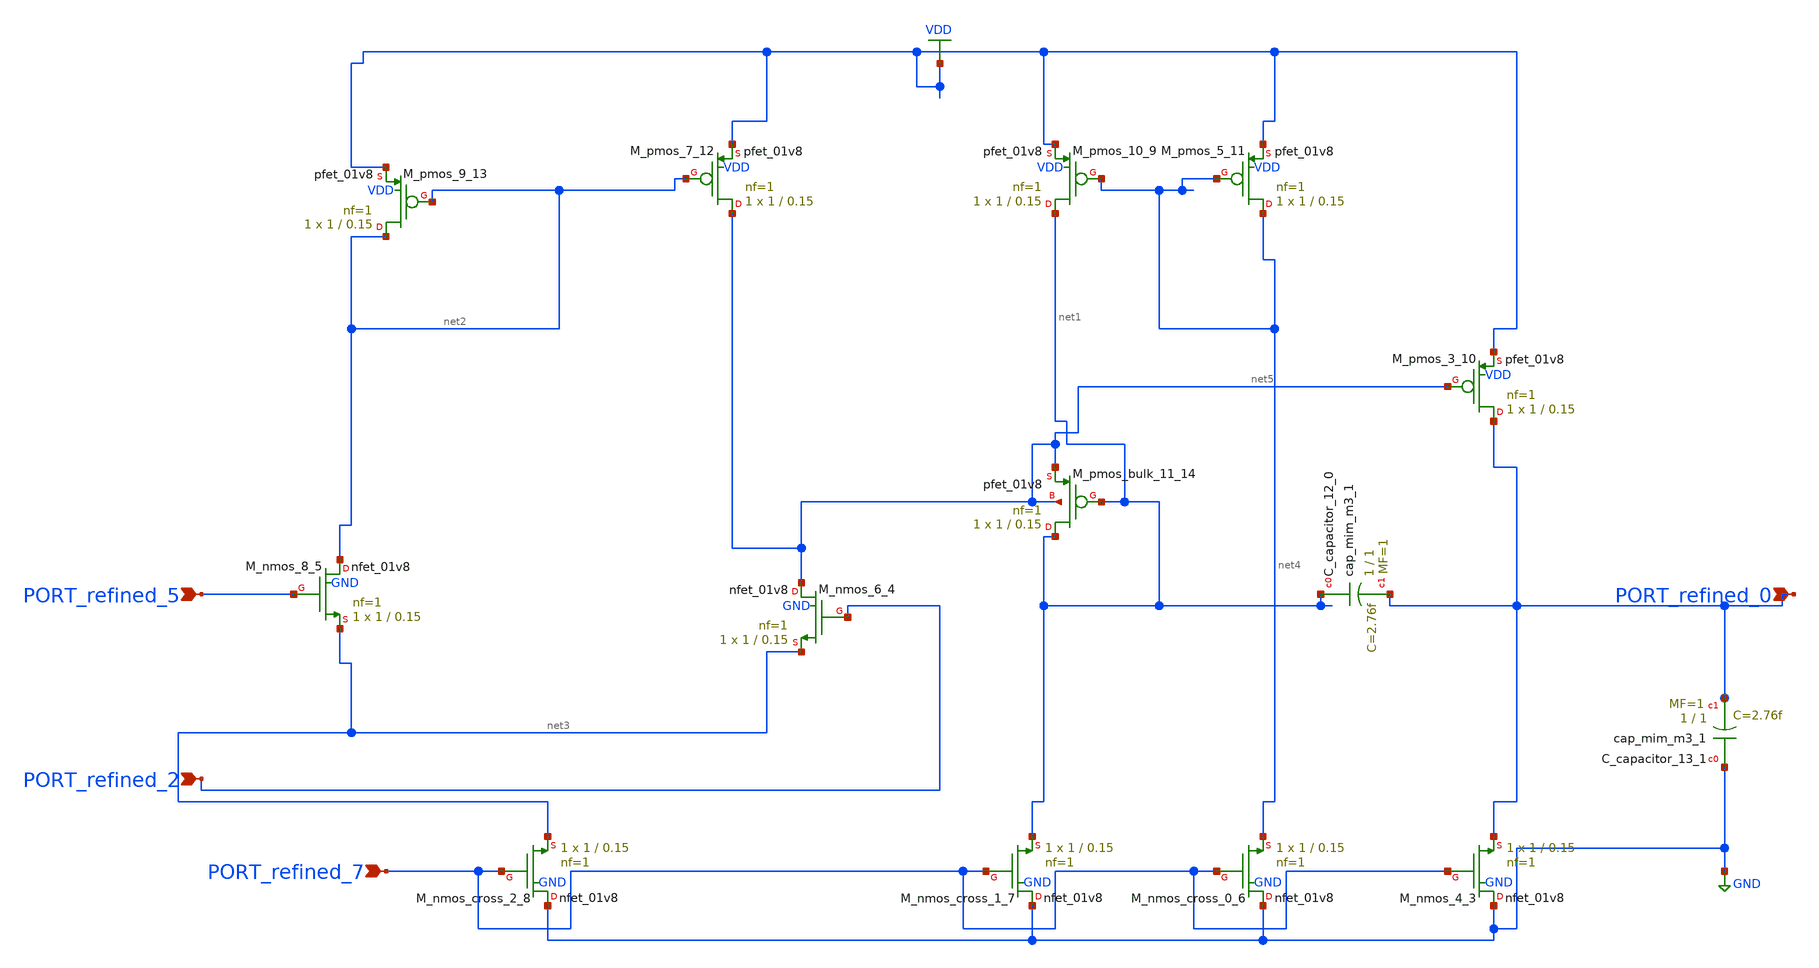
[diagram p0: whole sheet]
** sch_path: schematics/Image2Net/070.sch
**.subckt 070 PORT_refined_0 PORT_refined_2 PORT_refined_5 PORT_refined_7
*.ipin PORT_refined_0
*.ipin PORT_refined_2
*.ipin PORT_refined_5
*.ipin PORT_refined_7
XC_capacitor_12_0 net1 PORT_refined_0 sky130_fd_pr__cap_mim_m3_1 W=1 L=1 MF=1 m=1
XC_capacitor_13_1 GND PORT_refined_0 sky130_fd_pr__cap_mim_m3_1 W=1 L=1 MF=1 m=1
XM_nmos_4_3 GND PORT_refined_7 PORT_refined_0 GND sky130_fd_pr__nfet_01v8 L=0.15 W=1 nf=1 ad='int((1 + 1)/2) * 1 / 1 * 0.29'
+ as='int((1 + 2)/2) * 1 / 1 * 0.29' pd='2*int((1 + 1)/2) * (1 / 1 + 0.29)' ps='2*int((1 + 2)/2) * (1 / 1 + 0.29)'
+ nrd='0.29 / 1 ' nrs='0.29 / 1 ' sa=0 sb=0 sd=0 mult=1 m=1
XM_nmos_6_4 net5 PORT_refined_2 net3 GND sky130_fd_pr__nfet_01v8 L=0.15 W=1 nf=1 ad='int((1 + 1)/2) * 1 / 1 * 0.29'
+ as='int((1 + 2)/2) * 1 / 1 * 0.29' pd='2*int((1 + 1)/2) * (1 / 1 + 0.29)' ps='2*int((1 + 2)/2) * (1 / 1 + 0.29)'
+ nrd='0.29 / 1 ' nrs='0.29 / 1 ' sa=0 sb=0 sd=0 mult=1 m=1
XM_nmos_8_5 net2 PORT_refined_5 net3 GND sky130_fd_pr__nfet_01v8 L=0.15 W=1 nf=1 ad='int((1 + 1)/2) * 1 / 1 * 0.29'
+ as='int((1 + 2)/2) * 1 / 1 * 0.29' pd='2*int((1 + 1)/2) * (1 / 1 + 0.29)' ps='2*int((1 + 2)/2) * (1 / 1 + 0.29)'
+ nrd='0.29 / 1 ' nrs='0.29 / 1 ' sa=0 sb=0 sd=0 mult=1 m=1
XM_nmos_cross_0_6 GND PORT_refined_7 net4 GND sky130_fd_pr__nfet_01v8 L=0.15 W=1 nf=1 ad='int((1 + 1)/2) * 1 / 1 * 0.29'
+ as='int((1 + 2)/2) * 1 / 1 * 0.29' pd='2*int((1 + 1)/2) * (1 / 1 + 0.29)' ps='2*int((1 + 2)/2) * (1 / 1 + 0.29)'
+ nrd='0.29 / 1 ' nrs='0.29 / 1 ' sa=0 sb=0 sd=0 mult=1 m=1
XM_nmos_cross_1_7 GND PORT_refined_7 net1 GND sky130_fd_pr__nfet_01v8 L=0.15 W=1 nf=1 ad='int((1 + 1)/2) * 1 / 1 * 0.29'
+ as='int((1 + 2)/2) * 1 / 1 * 0.29' pd='2*int((1 + 1)/2) * (1 / 1 + 0.29)' ps='2*int((1 + 2)/2) * (1 / 1 + 0.29)'
+ nrd='0.29 / 1 ' nrs='0.29 / 1 ' sa=0 sb=0 sd=0 mult=1 m=1
XM_nmos_cross_2_8 GND PORT_refined_7 net3 GND sky130_fd_pr__nfet_01v8 L=0.15 W=1 nf=1 ad='int((1 + 1)/2) * 1 / 1 * 0.29'
+ as='int((1 + 2)/2) * 1 / 1 * 0.29' pd='2*int((1 + 1)/2) * (1 / 1 + 0.29)' ps='2*int((1 + 2)/2) * (1 / 1 + 0.29)'
+ nrd='0.29 / 1 ' nrs='0.29 / 1 ' sa=0 sb=0 sd=0 mult=1 m=1
XM_pmos_10_9 net1 net4 VDD VDD sky130_fd_pr__pfet_01v8 L=0.15 W=1 nf=1 ad='int((1 + 1)/2) * 1 / 1 * 0.29'
+ as='int((1 + 2)/2) * 1 / 1 * 0.29' pd='2*int((1 + 1)/2) * (1 / 1 + 0.29)' ps='2*int((1 + 2)/2) * (1 / 1 + 0.29)'
+ nrd='0.29 / 1 ' nrs='0.29 / 1 ' sa=0 sb=0 sd=0 mult=1 m=1
XM_pmos_3_10 PORT_refined_0 net5 VDD VDD sky130_fd_pr__pfet_01v8 L=0.15 W=1 nf=1 ad='int((1 + 1)/2) * 1 / 1 * 0.29'
+ as='int((1 + 2)/2) * 1 / 1 * 0.29' pd='2*int((1 + 1)/2) * (1 / 1 + 0.29)' ps='2*int((1 + 2)/2) * (1 / 1 + 0.29)'
+ nrd='0.29 / 1 ' nrs='0.29 / 1 ' sa=0 sb=0 sd=0 mult=1 m=1
XM_pmos_5_11 net4 net4 VDD VDD sky130_fd_pr__pfet_01v8 L=0.15 W=1 nf=1 ad='int((1 + 1)/2) * 1 / 1 * 0.29'
+ as='int((1 + 2)/2) * 1 / 1 * 0.29' pd='2*int((1 + 1)/2) * (1 / 1 + 0.29)' ps='2*int((1 + 2)/2) * (1 / 1 + 0.29)'
+ nrd='0.29 / 1 ' nrs='0.29 / 1 ' sa=0 sb=0 sd=0 mult=1 m=1
XM_pmos_7_12 net5 net2 VDD VDD sky130_fd_pr__pfet_01v8 L=0.15 W=1 nf=1 ad='int((1 + 1)/2) * 1 / 1 * 0.29'
+ as='int((1 + 2)/2) * 1 / 1 * 0.29' pd='2*int((1 + 1)/2) * (1 / 1 + 0.29)' ps='2*int((1 + 2)/2) * (1 / 1 + 0.29)'
+ nrd='0.29 / 1 ' nrs='0.29 / 1 ' sa=0 sb=0 sd=0 mult=1 m=1
XM_pmos_9_13 net2 net2 VDD VDD sky130_fd_pr__pfet_01v8 L=0.15 W=1 nf=1 ad='int((1 + 1)/2) * 1 / 1 * 0.29'
+ as='int((1 + 2)/2) * 1 / 1 * 0.29' pd='2*int((1 + 1)/2) * (1 / 1 + 0.29)' ps='2*int((1 + 2)/2) * (1 / 1 + 0.29)'
+ nrd='0.29 / 1 ' nrs='0.29 / 1 ' sa=0 sb=0 sd=0 mult=1 m=1
XM_pmos_bulk_11_14 net1 net1 net5 net5 sky130_fd_pr__pfet_01v8 L=0.15 W=1 nf=1 ad='int((1 + 1)/2) * 1 / 1 * 0.29'
+ as='int((1 + 2)/2) * 1 / 1 * 0.29' pd='2*int((1 + 1)/2) * (1 / 1 + 0.29)' ps='2*int((1 + 2)/2) * (1 / 1 + 0.29)'
+ nrd='0.29 / 1 ' nrs='0.29 / 1 ' sa=0 sb=0 sd=0 mult=1 m=1
**.ends
.GLOBAL GND
.GLOBAL VDD
.end
